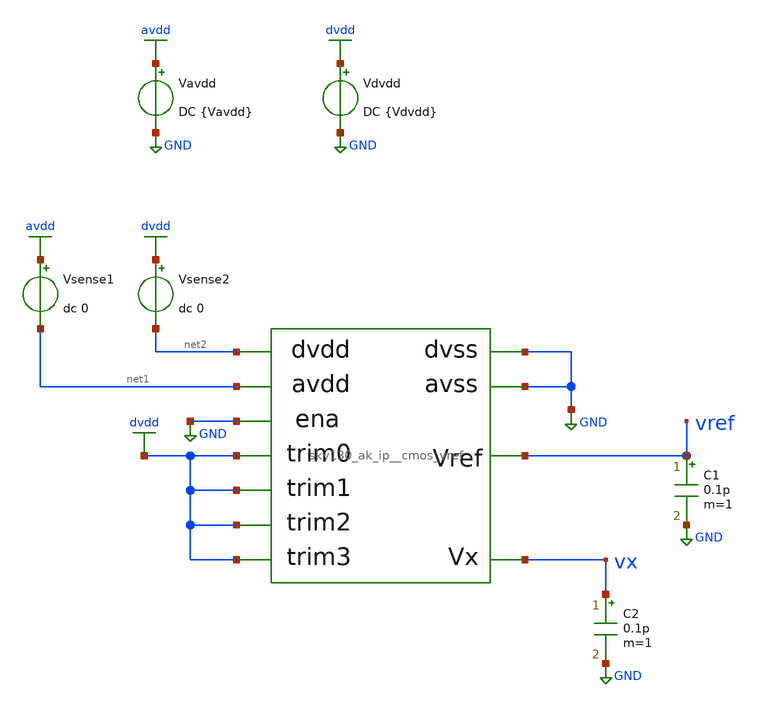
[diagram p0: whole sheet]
** sch_path: cace/tb_temp_coeff.sch
**.subckt tb_temp_coeff
Vavdd avdd GND DC {Vavdd}
X1 net1 GND dvdd vref vx dvdd dvdd dvdd net2 GND GND sky130_ak_ip__cmos_vref
Vsense1 avdd net1 dc 0
C2 vx GND 0.1p m=1
Vdvdd dvdd GND DC {Vdvdd}
C1 vref GND 0.1p m=1
Vsense2 dvdd net2 dc 0
**** begin user architecture code


.control
dc TEMP -40 85 5

let temp_diff = {temperature|maximum}-{temperature|minimum}
let vref_diff = maximum(vref)-minimum(vref)
let vref_nom = (maximum(vref)+minimum(vref))/2
let temp_coeff = vref_diff/(vref_nom*temp_diff)

print CEIL(temp_coeff)

echo $&temp_coeff > {simpath}/{filename}_{N}.data

quit
.endc




.lib /usr/local/share/pdk/sky130A/libs.tech/combined/sky130.lib.spice {corner}
.option warn=1


**** end user architecture code
**.ends

* expanding   symbol:  /home/moduhub/work/sky130_ak_ip__cmos_vref/xschem/sky130_ak_ip__cmos_vref.sym
*+ # of pins=11
** sym_path: xschem/sky130_ak_ip__cmos_vref.sym
** sch_path: xschem/sky130_ak_ip__cmos_vref.sch
.subckt sky130_ak_ip__cmos_vref avdd avss trim0 vref vx trim1 trim2 trim3 dvdd dvss ena
*.opin vref
*.iopin avss
*.iopin avdd
*.opin vx
*.ipin trim0
*.ipin trim1
*.ipin trim2
*.ipin trim3
*.iopin dvdd
*.iopin dvss
*.iopin avdd
*.ipin ena
XM3 net1 net3 vx GND sky130_fd_pr__nfet_g5v0d10v5 L=1 W=100 nf=5 ad='int((nf+1)/2) * W/nf * 0.29' as='int((nf+2)/2) * W/nf * 0.29'
+ pd='2*int((nf+1)/2) * (W/nf + 0.29)' ps='2*int((nf+2)/2) * (W/nf + 0.29)' nrd='0.29 / W' nrs='0.29 / W'
+ sa=0 sb=0 sd=0 mult=1 m=1
XM4 net2 net3 avss GND sky130_fd_pr__nfet_g5v0d10v5 L=1 W=5 nf=1 ad='int((nf+1)/2) * W/nf * 0.29' as='int((nf+2)/2) * W/nf * 0.29'
+ pd='2*int((nf+1)/2) * (W/nf + 0.29)' ps='2*int((nf+2)/2) * (W/nf + 0.29)' nrd='0.29 / W' nrs='0.29 / W'
+ sa=0 sb=0 sd=0 mult=1 m=1
XM5 net4 vref net1 GND sky130_fd_pr__nfet_g5v0d10v5 L=10 W=10 nf=1 ad='int((nf+1)/2) * W/nf * 0.29' as='int((nf+2)/2) * W/nf * 0.29'
+ pd='2*int((nf+1)/2) * (W/nf + 0.29)' ps='2*int((nf+2)/2) * (W/nf + 0.29)' nrd='0.29 / W' nrs='0.29 / W'
+ sa=0 sb=0 sd=0 mult=1 m=1
XM6 net3 vref net2 GND sky130_fd_pr__nfet_g5v0d10v5 L=10 W=10 nf=1 ad='int((nf+1)/2) * W/nf * 0.29' as='int((nf+2)/2) * W/nf * 0.29'
+ pd='2*int((nf+1)/2) * (W/nf + 0.29)' ps='2*int((nf+2)/2) * (W/nf + 0.29)' nrd='0.29 / W' nrs='0.29 / W'
+ sa=0 sb=0 sd=0 mult=1 m=1
XM7 net4 net4 avdd_ena avdd sky130_fd_pr__pfet_g5v0d10v5 L=10 W=5 nf=1 ad='int((nf+1)/2) * W/nf * 0.29'
+ as='int((nf+2)/2) * W/nf * 0.29' pd='2*int((nf+1)/2) * (W/nf + 0.29)' ps='2*int((nf+2)/2) * (W/nf + 0.29)'
+ nrd='0.29 / W' nrs='0.29 / W' sa=0 sb=0 sd=0 mult=1 m=1
XM8 net3 net4 avdd_ena avdd sky130_fd_pr__pfet_g5v0d10v5 L=10 W=5 nf=1 ad='int((nf+1)/2) * W/nf * 0.29'
+ as='int((nf+2)/2) * W/nf * 0.29' pd='2*int((nf+1)/2) * (W/nf + 0.29)' ps='2*int((nf+2)/2) * (W/nf + 0.29)'
+ nrd='0.29 / W' nrs='0.29 / W' sa=0 sb=0 sd=0 mult=1 m=1
XM9 vref net4 avdd_ena avdd sky130_fd_pr__pfet_g5v0d10v5 L=10 W=50 nf=1 ad='int((nf+1)/2) * W/nf * 0.29'
+ as='int((nf+2)/2) * W/nf * 0.29' pd='2*int((nf+1)/2) * (W/nf + 0.29)' ps='2*int((nf+2)/2) * (W/nf + 0.29)'
+ nrd='0.29 / W' nrs='0.29 / W' sa=0 sb=0 sd=0 mult=1 m=1
XM10 net5 net3 avss GND sky130_fd_pr__nfet_g5v0d10v5 L=1 W=5 nf=1 ad='int((nf+1)/2) * W/nf * 0.29' as='int((nf+2)/2) * W/nf * 0.29'
+ pd='2*int((nf+1)/2) * (W/nf + 0.29)' ps='2*int((nf+2)/2) * (W/nf + 0.29)' nrd='0.29 / W' nrs='0.29 / W'
+ sa=0 sb=0 sd=0 mult=1 m=1
XM11 net4 net5 avss GND sky130_fd_pr__nfet_g5v0d10v5 L=1 W=5 nf=1 ad='int((nf+1)/2) * W/nf * 0.29' as='int((nf+2)/2) * W/nf * 0.29'
+ pd='2*int((nf+1)/2) * (W/nf + 0.29)' ps='2*int((nf+2)/2) * (W/nf + 0.29)' nrd='0.29 / W' nrs='0.29 / W'
+ sa=0 sb=0 sd=0 mult=1 m=1
XC1 avdd_ena net5 sky130_fd_pr__cap_mim_m3_1 W=5 L=5 MF=1 m=1
XM12 vref net4 net9 avdd sky130_fd_pr__pfet_g5v0d10v5 L=10 W=1 nf=1 ad='int((nf+1)/2) * W/nf * 0.29'
+ as='int((nf+2)/2) * W/nf * 0.29' pd='2*int((nf+1)/2) * (W/nf + 0.29)' ps='2*int((nf+2)/2) * (W/nf + 0.29)'
+ nrd='0.29 / W' nrs='0.29 / W' sa=0 sb=0 sd=0 mult=1 m=1
XM13 vref net4 net8 avdd sky130_fd_pr__pfet_g5v0d10v5 L=10 W=2 nf=1 ad='int((nf+1)/2) * W/nf * 0.29'
+ as='int((nf+2)/2) * W/nf * 0.29' pd='2*int((nf+1)/2) * (W/nf + 0.29)' ps='2*int((nf+2)/2) * (W/nf + 0.29)'
+ nrd='0.29 / W' nrs='0.29 / W' sa=0 sb=0 sd=0 mult=1 m=1
XM14 net9 trim0 avdd_ena dvdd sky130_fd_pr__pfet_g5v0d10v5 L=0.15 W=1 nf=1 ad='int((nf+1)/2) * W/nf * 0.29'
+ as='int((nf+2)/2) * W/nf * 0.29' pd='2*int((nf+1)/2) * (W/nf + 0.29)' ps='2*int((nf+2)/2) * (W/nf + 0.29)'
+ nrd='0.29 / W' nrs='0.29 / W' sa=0 sb=0 sd=0 mult=1 m=1
XM15 net8 trim1 avdd_ena dvdd sky130_fd_pr__pfet_g5v0d10v5 L=0.15 W=1 nf=1 ad='int((nf+1)/2) * W/nf * 0.29'
+ as='int((nf+2)/2) * W/nf * 0.29' pd='2*int((nf+1)/2) * (W/nf + 0.29)' ps='2*int((nf+2)/2) * (W/nf + 0.29)'
+ nrd='0.29 / W' nrs='0.29 / W' sa=0 sb=0 sd=0 mult=1 m=1
XM16 vref net4 net7 avdd sky130_fd_pr__pfet_g5v0d10v5 L=10 W=4 nf=1 ad='int((nf+1)/2) * W/nf * 0.29'
+ as='int((nf+2)/2) * W/nf * 0.29' pd='2*int((nf+1)/2) * (W/nf + 0.29)' ps='2*int((nf+2)/2) * (W/nf + 0.29)'
+ nrd='0.29 / W' nrs='0.29 / W' sa=0 sb=0 sd=0 mult=1 m=1
XM17 net7 trim2 avdd_ena dvdd sky130_fd_pr__pfet_g5v0d10v5 L=0.15 W=1 nf=1 ad='int((nf+1)/2) * W/nf * 0.29'
+ as='int((nf+2)/2) * W/nf * 0.29' pd='2*int((nf+1)/2) * (W/nf + 0.29)' ps='2*int((nf+2)/2) * (W/nf + 0.29)'
+ nrd='0.29 / W' nrs='0.29 / W' sa=0 sb=0 sd=0 mult=1 m=1
XM18 vref net4 net6 avdd sky130_fd_pr__pfet_g5v0d10v5 L=10 W=8 nf=1 ad='int((nf+1)/2) * W/nf * 0.29'
+ as='int((nf+2)/2) * W/nf * 0.29' pd='2*int((nf+1)/2) * (W/nf + 0.29)' ps='2*int((nf+2)/2) * (W/nf + 0.29)'
+ nrd='0.29 / W' nrs='0.29 / W' sa=0 sb=0 sd=0 mult=1 m=1
XM19 net6 trim3 avdd_ena dvdd sky130_fd_pr__pfet_g5v0d10v5 L=0.15 W=1 nf=1 ad='int((nf+1)/2) * W/nf * 0.29'
+ as='int((nf+2)/2) * W/nf * 0.29' pd='2*int((nf+1)/2) * (W/nf + 0.29)' ps='2*int((nf+2)/2) * (W/nf + 0.29)'
+ nrd='0.29 / W' nrs='0.29 / W' sa=0 sb=0 sd=0 mult=1 m=1
XM1 vx vref avss GND sky130_fd_pr__nfet_g5v0d10v5 L=10 W=2.5 nf=1 ad='int((nf+1)/2) * W/nf * 0.29' as='int((nf+2)/2) * W/nf * 0.29'
+ pd='2*int((nf+1)/2) * (W/nf + 0.29)' ps='2*int((nf+2)/2) * (W/nf + 0.29)' nrd='0.29 / W' nrs='0.29 / W'
+ sa=0 sb=0 sd=0 mult=1 m=1
XM2 vref vref vx GND sky130_fd_pr__nfet_g5v0d10v5 L=10 W=2 nf=1 ad='int((nf+1)/2) * W/nf * 0.29' as='int((nf+2)/2) * W/nf * 0.29'
+ pd='2*int((nf+1)/2) * (W/nf + 0.29)' ps='2*int((nf+2)/2) * (W/nf + 0.29)' nrd='0.29 / W' nrs='0.29 / W'
+ sa=0 sb=0 sd=0 mult=1 m=1
XM20 avdd_ena ena avdd dvdd sky130_fd_pr__pfet_g5v0d10v5 L=0.3 W=5 nf=1 ad='int((nf+1)/2) * W/nf * 0.29'
+ as='int((nf+2)/2) * W/nf * 0.29' pd='2*int((nf+1)/2) * (W/nf + 0.29)' ps='2*int((nf+2)/2) * (W/nf + 0.29)'
+ nrd='0.29 / W' nrs='0.29 / W' sa=0 sb=0 sd=0 mult=1 m=1
.ends

.GLOBAL avdd
.GLOBAL GND
.GLOBAL dvdd
.end
